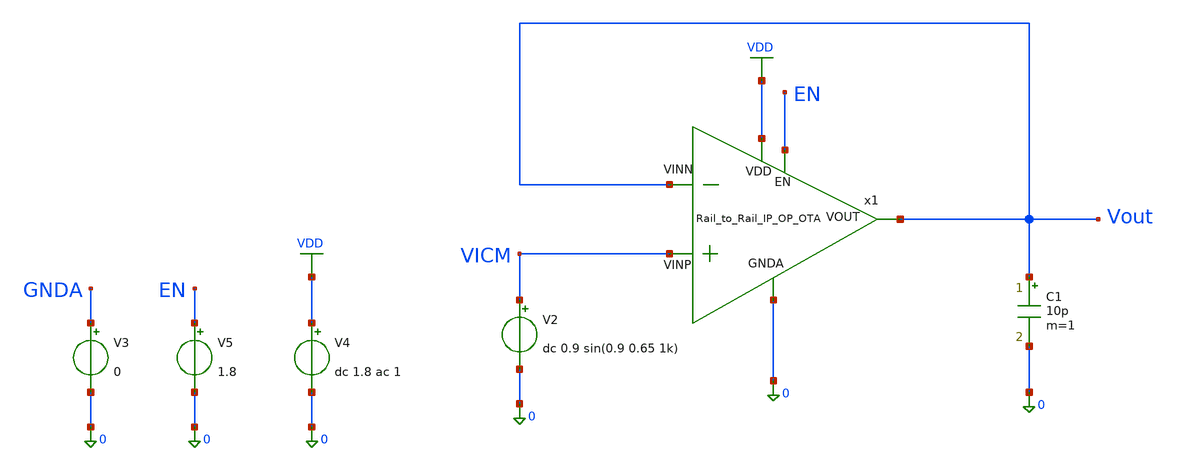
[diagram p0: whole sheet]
** sch_path: OTAs/Rail_to_Rail_OTA_Inp_IP/without_internal_bias/SCH/Rail_to_Rail_IP_OP_OTA_MC.sch
.lib $::SKYWATER_MODELS/sky130.lib.spice tt
.include $::SKYWATER_STDCELLS/sky130_fd_sc_hd.spice

**.subckt Rail_to_Rail_IP_OP_OTA_MC
V3 GNDA 0 0
V5 EN 0 1.8
C1 Vout 0 10p m=1
x1 VDD VICM Vout Vout EN 0 Rail_to_Rail_IP_OP_OTA
V2 VICM 0 dc 0.9 sin(0.9 0.65 1k)
V4 VDD 0 dc 1.8 ac 1
**** begin user architecture code



.save @m.x1.xmn_bot_l2.msky130_fd_pr__nfet_01v8[gm]
.save @m.x1.xmn_bot_l2.msky130_fd_pr__nfet_01v8[gds]
.save @m.x1.xmn_bot_l2.msky130_fd_pr__nfet_01v8[vth]
.save @m.x1.xmn_bot_l2.msky130_fd_pr__nfet_01v8[vdsat]
.save @m.x1.xmn_bot_l2.msky130_fd_pr__nfet_01v8[cgg]
.save @m.x1.xmn_bot_l2.msky130_fd_pr__nfet_01v8[cgso]
.save @m.x1.xmn_bot_l2.msky130_fd_pr__nfet_01v8[cgdo]
.save @m.x1.xmn_casc_l2.msky130_fd_pr__nfet_01v8[gm]
.save @m.x1.xmn_casc_l2.msky130_fd_pr__nfet_01v8[gds]
.save @m.x1.xmn_casc_l2.msky130_fd_pr__nfet_01v8[vth]
.save @m.x1.xmn_casc_l2.msky130_fd_pr__nfet_01v8[vdsat]
.save @m.x1.xmn_casc_l2.msky130_fd_pr__nfet_01v8[cgg]
.save @m.x1.xmn_casc_l2.msky130_fd_pr__nfet_01v8[cgso]
.save @m.x1.xmn_casc_l2.msky130_fd_pr__nfet_01v8[cgdo]
.save @m.x1.xmn_bot_l1.msky130_fd_pr__nfet_01v8[gm]
.save @m.x1.xmn_bot_l1.msky130_fd_pr__nfet_01v8[gds]
.save @m.x1.xmn_bot_l1.msky130_fd_pr__nfet_01v8[vth]
.save @m.x1.xmn_bot_l1.msky130_fd_pr__nfet_01v8[vdsat]
.save @m.x1.xmn_bot_l1.msky130_fd_pr__nfet_01v8[cgg]
.save @m.x1.xmn_bot_l1.msky130_fd_pr__nfet_01v8[cgso]
.save @m.x1.xmn_bot_l1.msky130_fd_pr__nfet_01v8[cgdo]
.save @m.x1.xmn_casc_l1.msky130_fd_pr__nfet_01v8[gm]
.save @m.x1.xmn_casc_l1.msky130_fd_pr__nfet_01v8[gds]
.save @m.x1.xmn_casc_l1.msky130_fd_pr__nfet_01v8[vth]
.save @m.x1.xmn_casc_l1.msky130_fd_pr__nfet_01v8[vdsat]
.save @m.x1.xmn_casc_l1.msky130_fd_pr__nfet_01v8[cgg]
.save @m.x1.xmn_casc_l1.msky130_fd_pr__nfet_01v8[cgso]
.save @m.x1.xmn_casc_l1.msky130_fd_pr__nfet_01v8[cgdo]
.save @m.x1.xmp_casc_l2.msky130_fd_pr__pfet_01v8[gm]
.save @m.x1.xmp_casc_l2.msky130_fd_pr__pfet_01v8[gds]
.save @m.x1.xmp_casc_l2.msky130_fd_pr__pfet_01v8[vth]
.save @m.x1.xmp_casc_l2.msky130_fd_pr__pfet_01v8[vdsat]
.save @m.x1.xmp_casc_l2.msky130_fd_pr__pfet_01v8[cgg]
.save @m.x1.xmp_casc_l2.msky130_fd_pr__pfet_01v8[cgso]
.save @m.x1.xmp_casc_l2.msky130_fd_pr__pfet_01v8[cgdo]
.save @m.x1.xmp_casc_l1.msky130_fd_pr__pfet_01v8[gm]
.save @m.x1.xmp_casc_l1.msky130_fd_pr__pfet_01v8[gds]
.save @m.x1.xmp_casc_l1.msky130_fd_pr__pfet_01v8[vth]
.save @m.x1.xmp_casc_l1.msky130_fd_pr__pfet_01v8[vdsat]
.save @m.x1.xmp_casc_l1.msky130_fd_pr__pfet_01v8[cgg]
.save @m.x1.xmp_casc_l1.msky130_fd_pr__pfet_01v8[cgso]
.save @m.x1.xmp_casc_l1.msky130_fd_pr__pfet_01v8[cgdo]
.save @m.x1.xmp_top_l1.msky130_fd_pr__pfet_01v8[gm]
.save @m.x1.xmp_top_l1.msky130_fd_pr__pfet_01v8[gds]
.save @m.x1.xmp_top_l1.msky130_fd_pr__pfet_01v8[vth]
.save @m.x1.xmp_top_l1.msky130_fd_pr__pfet_01v8[vdsat]
.save @m.x1.xmp_top_l1.msky130_fd_pr__pfet_01v8[cgg]
.save @m.x1.xmp_top_l1.msky130_fd_pr__pfet_01v8[cgso]
.save @m.x1.xmp_top_l1.msky130_fd_pr__pfet_01v8[cgdo]
.save @m.x1.xmn_a1.msky130_fd_pr__nfet_01v8_lvt[gm]
.save @m.x1.xmn_a1.msky130_fd_pr__nfet_01v8_lvt[gds]
.save @m.x1.xmn_a1.msky130_fd_pr__nfet_01v8_lvt[vth]
.save @m.x1.xmn_a1.msky130_fd_pr__nfet_01v8_lvt[vdsat]
.save @m.x1.xmn_a1.msky130_fd_pr__nfet_01v8_lvt[cgg]
.save @m.x1.xmn_a1.msky130_fd_pr__nfet_01v8_lvt[cgso]
.save @m.x1.xmn_a1.msky130_fd_pr__nfet_01v8_lvt[cgdo]
.save @m.x1.xmn_a2.msky130_fd_pr__nfet_01v8_lvt[gm]
.save @m.x1.xmn_a2.msky130_fd_pr__nfet_01v8_lvt[gds]
.save @m.x1.xmn_a2.msky130_fd_pr__nfet_01v8_lvt[vth]
.save @m.x1.xmn_a2.msky130_fd_pr__nfet_01v8_lvt[vdsat]
.save @m.x1.xmn_a2.msky130_fd_pr__nfet_01v8_lvt[cgg]
.save @m.x1.xmn_a2.msky130_fd_pr__nfet_01v8_lvt[cgso]
.save @m.x1.xmn_a2.msky130_fd_pr__nfet_01v8_lvt[cgdo]
.save @m.x1.xmp_a1.msky130_fd_pr__pfet_01v8_lvt[gm]
.save @m.x1.xmp_a1.msky130_fd_pr__pfet_01v8_lvt[gds]
.save @m.x1.xmp_a1.msky130_fd_pr__pfet_01v8_lvt[vth]
.save @m.x1.xmp_a1.msky130_fd_pr__pfet_01v8_lvt[vdsat]
.save @m.x1.xmp_a1.msky130_fd_pr__pfet_01v8_lvt[cgg]
.save @m.x1.xmp_a1.msky130_fd_pr__pfet_01v8_lvt[cgso]
.save @m.x1.xmp_a1.msky130_fd_pr__pfet_01v8_lvt[cgdo]
.save @m.x1.xmp_a2.msky130_fd_pr__pfet_01v8_lvt[gm]
.save @m.x1.xmp_a2.msky130_fd_pr__pfet_01v8_lvt[gds]
.save @m.x1.xmp_a2.msky130_fd_pr__pfet_01v8_lvt[vth]
.save @m.x1.xmp_a2.msky130_fd_pr__pfet_01v8_lvt[vdsat]
.save @m.x1.xmp_a2.msky130_fd_pr__pfet_01v8_lvt[cgg]
.save @m.x1.xmp_a2.msky130_fd_pr__pfet_01v8_lvt[cgso]
.save @m.x1.xmp_a2.msky130_fd_pr__pfet_01v8_lvt[cgdo]
.save @m.x1.xmp_pdiff_bias.msky130_fd_pr__pfet_01v8[gm]
.save @m.x1.xmp_pdiff_bias.msky130_fd_pr__pfet_01v8[gds]
.save @m.x1.xmp_pdiff_bias.msky130_fd_pr__pfet_01v8[vth]
.save @m.x1.xmp_pdiff_bias.msky130_fd_pr__pfet_01v8[vdsat]
.save @m.x1.xmp_pdiff_bias.msky130_fd_pr__pfet_01v8[cgg]
.save @m.x1.xmp_pdiff_bias.msky130_fd_pr__pfet_01v8[cgso]
.save @m.x1.xmp_pdiff_bias.msky130_fd_pr__pfet_01v8[cgdo]
.save @m.x1.xmn_ndiff_bias.msky130_fd_pr__nfet_01v8[gm]
.save @m.x1.xmn_ndiff_bias.msky130_fd_pr__nfet_01v8[gds]
.save @m.x1.xmn_ndiff_bias.msky130_fd_pr__nfet_01v8[vth]
.save @m.x1.xmn_ndiff_bias.msky130_fd_pr__nfet_01v8[vdsat]
.save @m.x1.xmn_ndiff_bias.msky130_fd_pr__nfet_01v8[cgg]
.save @m.x1.xmn_ndiff_bias.msky130_fd_pr__nfet_01v8[cgso]
.save @m.x1.xmn_ndiff_bias.msky130_fd_pr__nfet_01v8[cgdo]
.save @m.x1.xmp_pdiff_bias_b.msky130_fd_pr__pfet_01v8[gm]
.save @m.x1.xmp_pdiff_bias_b.msky130_fd_pr__pfet_01v8[gds]
.save @m.x1.xmp_pdiff_bias_b.msky130_fd_pr__pfet_01v8[vth]
.save @m.x1.xmp_pdiff_bias_b.msky130_fd_pr__pfet_01v8[vdsat]
.save @m.x1.xmp_pdiff_bias_b.msky130_fd_pr__pfet_01v8[cgg]
.save @m.x1.xmp_pdiff_bias_b.msky130_fd_pr__pfet_01v8[cgso]
.save @m.x1.xmp_pdiff_bias_b.msky130_fd_pr__pfet_01v8[cgdo]
.save @m.x1.xmp_top_l2.msky130_fd_pr__pfet_01v8[gm]
.save @m.x1.xmp_top_l2.msky130_fd_pr__pfet_01v8[gds]
.save @m.x1.xmp_top_l2.msky130_fd_pr__pfet_01v8[vth]
.save @m.x1.xmp_top_l2.msky130_fd_pr__pfet_01v8[vdsat]
.save @m.x1.xmp_top_l2.msky130_fd_pr__pfet_01v8[cgg]
.save @m.x1.xmp_top_l2.msky130_fd_pr__pfet_01v8[cgso]
.save @m.x1.xmp_top_l2.msky130_fd_pr__pfet_01v8[cgdo]
.save @m.x1.xmn_bias_source.msky130_fd_pr__nfet_01v8[gm]
.save @m.x1.xmn_bias_source.msky130_fd_pr__nfet_01v8[gds]
.save @m.x1.xmn_bias_source.msky130_fd_pr__nfet_01v8[vth]
.save @m.x1.xmn_bias_source.msky130_fd_pr__nfet_01v8[vdsat]
.save @m.x1.xmn_bias_source.msky130_fd_pr__nfet_01v8[cgg]
.save @m.x1.xmn_bias_source.msky130_fd_pr__nfet_01v8[cgso]
.save @m.x1.xmn_bias_source.msky130_fd_pr__nfet_01v8[cgdo]
.save @m.x1.xmn_bias_ext.msky130_fd_pr__nfet_01v8[gm]
.save @m.x1.xmn_bias_ext.msky130_fd_pr__nfet_01v8[gds]
.save @m.x1.xmn_bias_ext.msky130_fd_pr__nfet_01v8[vth]
.save @m.x1.xmn_bias_ext.msky130_fd_pr__nfet_01v8[vdsat]
.save @m.x1.xmn_bias_ext.msky130_fd_pr__nfet_01v8[cgg]
.save @m.x1.xmn_bias_ext.msky130_fd_pr__nfet_01v8[cgso]
.save @m.x1.xmn_bias_ext.msky130_fd_pr__nfet_01v8[cgdo]
.save @m.x1.xmp_casc_b_source.msky130_fd_pr__pfet_01v8[gm]
.save @m.x1.xmp_casc_b_source.msky130_fd_pr__pfet_01v8[gds]
.save @m.x1.xmp_casc_b_source.msky130_fd_pr__pfet_01v8[vth]
.save @m.x1.xmp_casc_b_source.msky130_fd_pr__pfet_01v8[vdsat]
.save @m.x1.xmp_casc_b_source.msky130_fd_pr__pfet_01v8[cgg]
.save @m.x1.xmp_casc_b_source.msky130_fd_pr__pfet_01v8[cgso]
.save @m.x1.xmp_casc_b_source.msky130_fd_pr__pfet_01v8[cgdo]
.save @m.x1.xmn_casc_bias8.msky130_fd_pr__nfet_01v8[gm]
.save @m.x1.xmn_casc_bias8.msky130_fd_pr__nfet_01v8[gds]
.save @m.x1.xmn_casc_bias8.msky130_fd_pr__nfet_01v8[vth]
.save @m.x1.xmn_casc_bias8.msky130_fd_pr__nfet_01v8[vdsat]
.save @m.x1.xmn_casc_bias8.msky130_fd_pr__nfet_01v8[cgg]
.save @m.x1.xmn_casc_bias8.msky130_fd_pr__nfet_01v8[cgso]
.save @m.x1.xmn_casc_bias8.msky130_fd_pr__nfet_01v8[cgdo]
.save @m.x1.xmn_casc_b_source.msky130_fd_pr__nfet_01v8[gm]
.save @m.x1.xmn_casc_b_source.msky130_fd_pr__nfet_01v8[gds]
.save @m.x1.xmn_casc_b_source.msky130_fd_pr__nfet_01v8[vth]
.save @m.x1.xmn_casc_b_source.msky130_fd_pr__nfet_01v8[vdsat]
.save @m.x1.xmn_casc_b_source.msky130_fd_pr__nfet_01v8[cgg]
.save @m.x1.xmn_casc_b_source.msky130_fd_pr__nfet_01v8[cgso]
.save @m.x1.xmn_casc_b_source.msky130_fd_pr__nfet_01v8[cgdo]
.save @m.x1.xmp_casc_bias1.msky130_fd_pr__pfet_01v8[gm]
.save @m.x1.xmp_casc_bias1.msky130_fd_pr__pfet_01v8[gds]
.save @m.x1.xmp_casc_bias1.msky130_fd_pr__pfet_01v8[vth]
.save @m.x1.xmp_casc_bias1.msky130_fd_pr__pfet_01v8[vdsat]
.save @m.x1.xmp_casc_bias1.msky130_fd_pr__pfet_01v8[cgg]
.save @m.x1.xmp_casc_bias1.msky130_fd_pr__pfet_01v8[cgso]
.save @m.x1.xmp_casc_bias1.msky130_fd_pr__pfet_01v8[cgdo]
.save @m.x1.xmn_casc_bias7.msky130_fd_pr__nfet_01v8[gm]
.save @m.x1.xmn_casc_bias7.msky130_fd_pr__nfet_01v8[gds]
.save @m.x1.xmn_casc_bias7.msky130_fd_pr__nfet_01v8[vth]
.save @m.x1.xmn_casc_bias7.msky130_fd_pr__nfet_01v8[vdsat]
.save @m.x1.xmn_casc_bias7.msky130_fd_pr__nfet_01v8[cgg]
.save @m.x1.xmn_casc_bias7.msky130_fd_pr__nfet_01v8[cgso]
.save @m.x1.xmn_casc_bias7.msky130_fd_pr__nfet_01v8[cgdo]
.save @m.x1.xmn_casc_bias6.msky130_fd_pr__nfet_01v8[gm]
.save @m.x1.xmn_casc_bias6.msky130_fd_pr__nfet_01v8[gds]
.save @m.x1.xmn_casc_bias6.msky130_fd_pr__nfet_01v8[vth]
.save @m.x1.xmn_casc_bias6.msky130_fd_pr__nfet_01v8[vdsat]
.save @m.x1.xmn_casc_bias6.msky130_fd_pr__nfet_01v8[cgg]
.save @m.x1.xmn_casc_bias6.msky130_fd_pr__nfet_01v8[cgso]
.save @m.x1.xmn_casc_bias6.msky130_fd_pr__nfet_01v8[cgdo]
.save @m.x1.xmp_casc_bias2.msky130_fd_pr__pfet_01v8[gm]
.save @m.x1.xmp_casc_bias2.msky130_fd_pr__pfet_01v8[gds]
.save @m.x1.xmp_casc_bias2.msky130_fd_pr__pfet_01v8[vth]
.save @m.x1.xmp_casc_bias2.msky130_fd_pr__pfet_01v8[vdsat]
.save @m.x1.xmp_casc_bias2.msky130_fd_pr__pfet_01v8[cgg]
.save @m.x1.xmp_casc_bias2.msky130_fd_pr__pfet_01v8[cgso]
.save @m.x1.xmp_casc_bias2.msky130_fd_pr__pfet_01v8[cgdo]
.save @m.x1.xmp_casc_bias3.msky130_fd_pr__pfet_01v8[gm]
.save @m.x1.xmp_casc_bias3.msky130_fd_pr__pfet_01v8[gds]
.save @m.x1.xmp_casc_bias3.msky130_fd_pr__pfet_01v8[vth]
.save @m.x1.xmp_casc_bias3.msky130_fd_pr__pfet_01v8[vdsat]
.save @m.x1.xmp_casc_bias3.msky130_fd_pr__pfet_01v8[cgg]
.save @m.x1.xmp_casc_bias3.msky130_fd_pr__pfet_01v8[cgso]
.save @m.x1.xmp_casc_bias3.msky130_fd_pr__pfet_01v8[cgdo]
.save @m.x1.xmn_casc_bias5.msky130_fd_pr__nfet_01v8[gm]
.save @m.x1.xmn_casc_bias5.msky130_fd_pr__nfet_01v8[gds]
.save @m.x1.xmn_casc_bias5.msky130_fd_pr__nfet_01v8[vth]
.save @m.x1.xmn_casc_bias5.msky130_fd_pr__nfet_01v8[vdsat]
.save @m.x1.xmn_casc_bias5.msky130_fd_pr__nfet_01v8[cgg]
.save @m.x1.xmn_casc_bias5.msky130_fd_pr__nfet_01v8[cgso]
.save @m.x1.xmn_casc_bias5.msky130_fd_pr__nfet_01v8[cgdo]
.save @m.x1.xmn_casc_bias4.msky130_fd_pr__nfet_01v8[gm]
.save @m.x1.xmn_casc_bias4.msky130_fd_pr__nfet_01v8[gds]
.save @m.x1.xmn_casc_bias4.msky130_fd_pr__nfet_01v8[vth]
.save @m.x1.xmn_casc_bias4.msky130_fd_pr__nfet_01v8[vdsat]
.save @m.x1.xmn_casc_bias4.msky130_fd_pr__nfet_01v8[cgg]
.save @m.x1.xmn_casc_bias4.msky130_fd_pr__nfet_01v8[cgso]
.save @m.x1.xmn_casc_bias4.msky130_fd_pr__nfet_01v8[cgdo]
.save @m.x1.xmn_casc_bias3.msky130_fd_pr__nfet_01v8[gm]
.save @m.x1.xmn_casc_bias3.msky130_fd_pr__nfet_01v8[gds]
.save @m.x1.xmn_casc_bias3.msky130_fd_pr__nfet_01v8[vth]
.save @m.x1.xmn_casc_bias3.msky130_fd_pr__nfet_01v8[vdsat]
.save @m.x1.xmn_casc_bias3.msky130_fd_pr__nfet_01v8[cgg]
.save @m.x1.xmn_casc_bias3.msky130_fd_pr__nfet_01v8[cgso]
.save @m.x1.xmn_casc_bias3.msky130_fd_pr__nfet_01v8[cgdo]
.save @m.x1.xmn_casc_bias1.msky130_fd_pr__nfet_01v8[gm]
.save @m.x1.xmn_casc_bias1.msky130_fd_pr__nfet_01v8[gds]
.save @m.x1.xmn_casc_bias1.msky130_fd_pr__nfet_01v8[vth]
.save @m.x1.xmn_casc_bias1.msky130_fd_pr__nfet_01v8[vdsat]
.save @m.x1.xmn_casc_bias1.msky130_fd_pr__nfet_01v8[cgg]
.save @m.x1.xmn_casc_bias1.msky130_fd_pr__nfet_01v8[cgso]
.save @m.x1.xmn_casc_bias1.msky130_fd_pr__nfet_01v8[cgdo]
.save @m.x1.xmn_casc_bias2.msky130_fd_pr__nfet_01v8[gm]
.save @m.x1.xmn_casc_bias2.msky130_fd_pr__nfet_01v8[gds]
.save @m.x1.xmn_casc_bias2.msky130_fd_pr__nfet_01v8[vth]
.save @m.x1.xmn_casc_bias2.msky130_fd_pr__nfet_01v8[vdsat]
.save @m.x1.xmn_casc_bias2.msky130_fd_pr__nfet_01v8[cgg]
.save @m.x1.xmn_casc_bias2.msky130_fd_pr__nfet_01v8[cgso]
.save @m.x1.xmn_casc_bias2.msky130_fd_pr__nfet_01v8[cgdo]
.save @m.x1.xmn_sw1.msky130_fd_pr__nfet_01v8[gm]
.save @m.x1.xmn_sw1.msky130_fd_pr__nfet_01v8[gds]
.save @m.x1.xmn_sw1.msky130_fd_pr__nfet_01v8[vth]
.save @m.x1.xmn_sw1.msky130_fd_pr__nfet_01v8[vdsat]
.save @m.x1.xmn_sw1.msky130_fd_pr__nfet_01v8[cgg]
.save @m.x1.xmn_sw1.msky130_fd_pr__nfet_01v8[cgso]
.save @m.x1.xmn_sw1.msky130_fd_pr__nfet_01v8[cgdo]
.save @m.x1.xmp_sw1.msky130_fd_pr__pfet_01v8[gm]
.save @m.x1.xmp_sw1.msky130_fd_pr__pfet_01v8[gds]
.save @m.x1.xmp_sw1.msky130_fd_pr__pfet_01v8[vth]
.save @m.x1.xmp_sw1.msky130_fd_pr__pfet_01v8[vdsat]
.save @m.x1.xmp_sw1.msky130_fd_pr__pfet_01v8[cgg]
.save @m.x1.xmp_sw1.msky130_fd_pr__pfet_01v8[cgso]
.save @m.x1.xmp_sw1.msky130_fd_pr__pfet_01v8[cgdo]
.save @m.x1.xmp_sw2.msky130_fd_pr__pfet_01v8[gm]
.save @m.x1.xmp_sw2.msky130_fd_pr__pfet_01v8[gds]
.save @m.x1.xmp_sw2.msky130_fd_pr__pfet_01v8[vth]
.save @m.x1.xmp_sw2.msky130_fd_pr__pfet_01v8[vdsat]
.save @m.x1.xmp_sw2.msky130_fd_pr__pfet_01v8[cgg]
.save @m.x1.xmp_sw2.msky130_fd_pr__pfet_01v8[cgso]
.save @m.x1.xmp_sw2.msky130_fd_pr__pfet_01v8[cgdo]
.save @m.x1.xmn_sw2.msky130_fd_pr__nfet_01v8[gm]
.save @m.x1.xmn_sw2.msky130_fd_pr__nfet_01v8[gds]
.save @m.x1.xmn_sw2.msky130_fd_pr__nfet_01v8[vth]
.save @m.x1.xmn_sw2.msky130_fd_pr__nfet_01v8[vdsat]
.save @m.x1.xmn_sw2.msky130_fd_pr__nfet_01v8[cgg]
.save @m.x1.xmn_sw2.msky130_fd_pr__nfet_01v8[cgso]
.save @m.x1.xmn_sw2.msky130_fd_pr__nfet_01v8[cgdo]
.save @m.x1.xmp_sw3.msky130_fd_pr__pfet_01v8[gm]
.save @m.x1.xmp_sw3.msky130_fd_pr__pfet_01v8[gds]
.save @m.x1.xmp_sw3.msky130_fd_pr__pfet_01v8[vth]
.save @m.x1.xmp_sw3.msky130_fd_pr__pfet_01v8[vdsat]
.save @m.x1.xmp_sw3.msky130_fd_pr__pfet_01v8[cgg]
.save @m.x1.xmp_sw3.msky130_fd_pr__pfet_01v8[cgso]
.save @m.x1.xmp_sw3.msky130_fd_pr__pfet_01v8[cgdo]




.option gmin=1e-18
.options savecurrents
.save all
.temp=27
.control
 let runs=200
 let r=0
 dowhile r < runs
   reset
   let run=r
   op
   write /home/nithin/eda/LPCAS_TTSKY26a/tb_Gm_Cell_v2_MC_Sims_TB.raw
   set appendwrite
   let DIFF_MIS=v(VICM)-v(Vout)
   print v(DIFF_MIS)
   wrdata /home/nithin/eda/LPCAS_TTSKY26a/tb_Gm_Cell_v2_MC_Sims_TB.txt r v(DIFF_MIS)
   wrdata /home/nithin/eda/LPCAS_TTSKY26a/tb_Gm_Cell_v2_MC_Sims_TB.csv r v(DIFF_MIS)

   let r = r + 1
 end
.endc

**** end user architecture code
**.ends
.GLOBAL VDD
.end
